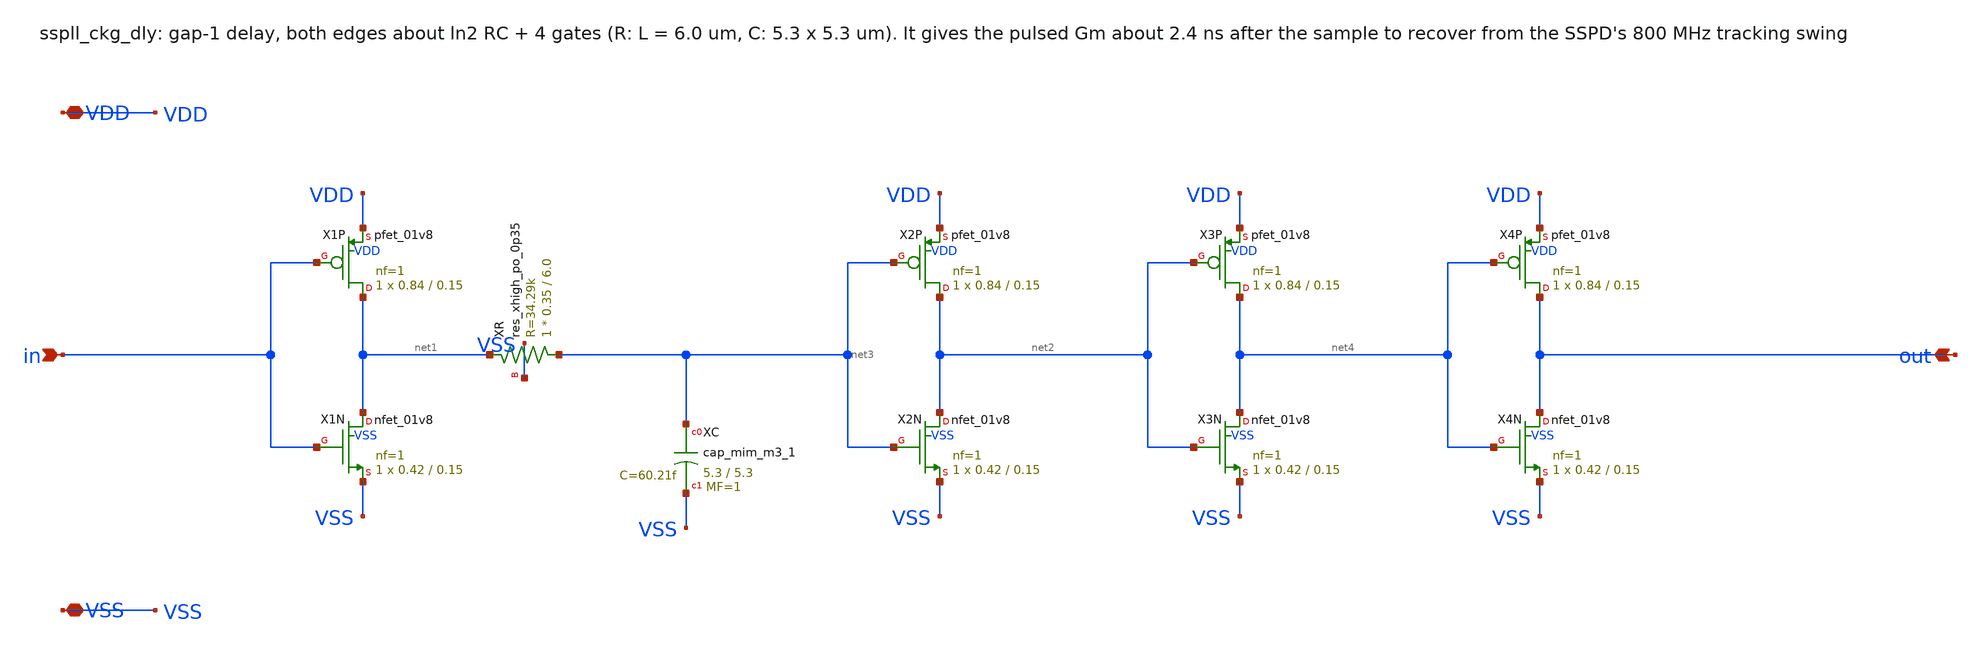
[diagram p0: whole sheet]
** sch_path: xschem/clkgen_hv/sspll_ckg_dly.sch
**.subckt sspll_ckg_dly in out VDD VSS
*.ipin in
*.opin out
*.iopin VDD
*.iopin VSS
XX1P net1 in VDD VDD sky130_fd_pr__pfet_01v8 L=0.15 W=0.84 nf=1 ad='int((nf+1)/2) * W/nf * 0.29' as='int((nf+2)/2) * W/nf * 0.29'
+ pd='2*int((nf+1)/2) * (W/nf + 0.29)' ps='2*int((nf+2)/2) * (W/nf + 0.29)' nrd='0.29 / W' nrs='0.29 / W'
+ sa=0 sb=0 sd=0 mult=1 m=1
XX1N net1 in VSS VSS sky130_fd_pr__nfet_01v8 L=0.15 W=0.42 nf=1 ad='int((nf+1)/2) * W/nf * 0.29' as='int((nf+2)/2) * W/nf * 0.29'
+ pd='2*int((nf+1)/2) * (W/nf + 0.29)' ps='2*int((nf+2)/2) * (W/nf + 0.29)' nrd='0.29 / W' nrs='0.29 / W'
+ sa=0 sb=0 sd=0 mult=1 m=1
XXR net3 net1 VSS sky130_fd_pr__res_xhigh_po_0p35 L=6.0 mult=1 m=1
XXC net3 VSS sky130_fd_pr__cap_mim_m3_1 W=5.3 L=5.3 MF=1 m=1
XX2P net2 net3 VDD VDD sky130_fd_pr__pfet_01v8 L=0.15 W=0.84 nf=1 ad='int((nf+1)/2) * W/nf * 0.29' as='int((nf+2)/2) * W/nf * 0.29'
+ pd='2*int((nf+1)/2) * (W/nf + 0.29)' ps='2*int((nf+2)/2) * (W/nf + 0.29)' nrd='0.29 / W' nrs='0.29 / W'
+ sa=0 sb=0 sd=0 mult=1 m=1
XX2N net2 net3 VSS VSS sky130_fd_pr__nfet_01v8 L=0.15 W=0.42 nf=1 ad='int((nf+1)/2) * W/nf * 0.29' as='int((nf+2)/2) * W/nf * 0.29'
+ pd='2*int((nf+1)/2) * (W/nf + 0.29)' ps='2*int((nf+2)/2) * (W/nf + 0.29)' nrd='0.29 / W' nrs='0.29 / W'
+ sa=0 sb=0 sd=0 mult=1 m=1
XX3P net4 net2 VDD VDD sky130_fd_pr__pfet_01v8 L=0.15 W=0.84 nf=1 ad='int((nf+1)/2) * W/nf * 0.29' as='int((nf+2)/2) * W/nf * 0.29'
+ pd='2*int((nf+1)/2) * (W/nf + 0.29)' ps='2*int((nf+2)/2) * (W/nf + 0.29)' nrd='0.29 / W' nrs='0.29 / W'
+ sa=0 sb=0 sd=0 mult=1 m=1
XX3N net4 net2 VSS VSS sky130_fd_pr__nfet_01v8 L=0.15 W=0.42 nf=1 ad='int((nf+1)/2) * W/nf * 0.29' as='int((nf+2)/2) * W/nf * 0.29'
+ pd='2*int((nf+1)/2) * (W/nf + 0.29)' ps='2*int((nf+2)/2) * (W/nf + 0.29)' nrd='0.29 / W' nrs='0.29 / W'
+ sa=0 sb=0 sd=0 mult=1 m=1
XX4P out net4 VDD VDD sky130_fd_pr__pfet_01v8 L=0.15 W=0.84 nf=1 ad='int((nf+1)/2) * W/nf * 0.29' as='int((nf+2)/2) * W/nf * 0.29'
+ pd='2*int((nf+1)/2) * (W/nf + 0.29)' ps='2*int((nf+2)/2) * (W/nf + 0.29)' nrd='0.29 / W' nrs='0.29 / W'
+ sa=0 sb=0 sd=0 mult=1 m=1
XX4N out net4 VSS VSS sky130_fd_pr__nfet_01v8 L=0.15 W=0.42 nf=1 ad='int((nf+1)/2) * W/nf * 0.29' as='int((nf+2)/2) * W/nf * 0.29'
+ pd='2*int((nf+1)/2) * (W/nf + 0.29)' ps='2*int((nf+2)/2) * (W/nf + 0.29)' nrd='0.29 / W' nrs='0.29 / W'
+ sa=0 sb=0 sd=0 mult=1 m=1
**.ends
.end
